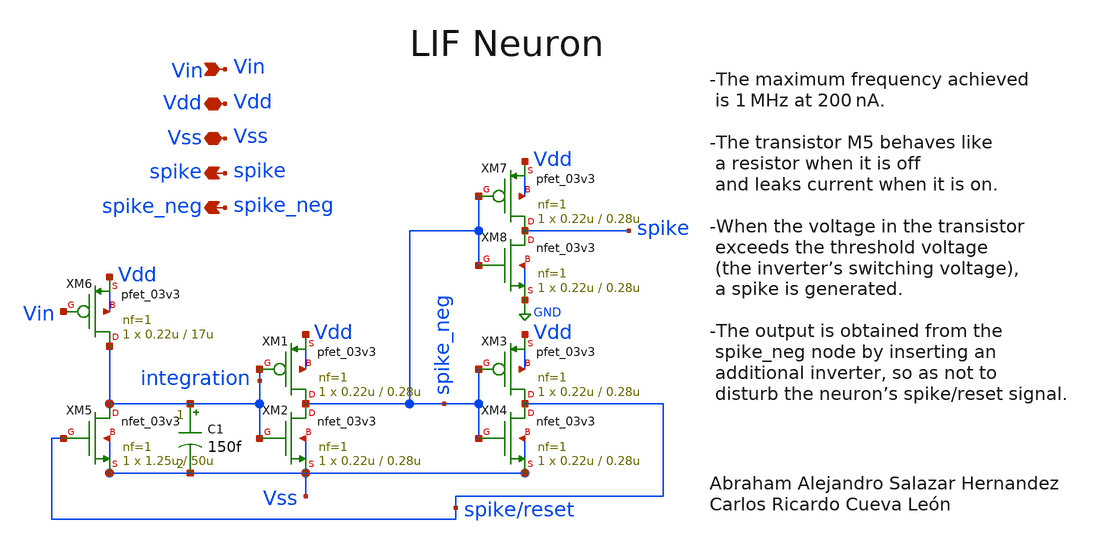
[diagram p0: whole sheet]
** sch_path: sch/lif/neurona.sch
**.subckt neurona Vdd Vss Vin spike spike_neg
*.iopin Vdd
*.iopin Vss
*.ipin Vin
*.opin spike
*.opin spike_neg
XM1 spike_neg integration Vdd Vdd pfet_03v3 L=0.28u W=0.22u nf=1 ad='int((nf+1)/2) * W/nf * 0.18u' as='int((nf+2)/2) * W/nf * 0.18u'
+ pd='2*int((nf+1)/2) * (W/nf + 0.18u)' ps='2*int((nf+2)/2) * (W/nf + 0.18u)' nrd='0.18u / W' nrs='0.18u / W'
+ sa=0 sb=0 sd=0 m=1
XM2 spike_neg integration Vss Vss nfet_03v3 L=0.28u W=0.22u nf=1 ad='int((nf+1)/2) * W/nf * 0.18u' as='int((nf+2)/2) * W/nf * 0.18u'
+ pd='2*int((nf+1)/2) * (W/nf + 0.18u)' ps='2*int((nf+2)/2) * (W/nf + 0.18u)' nrd='0.18u / W' nrs='0.18u / W'
+ sa=0 sb=0 sd=0 m=1
XM3 spike/reset spike_neg Vdd Vdd pfet_03v3 L=0.28u W=0.22u nf=1 ad='int((nf+1)/2) * W/nf * 0.18u' as='int((nf+2)/2) * W/nf * 0.18u'
+ pd='2*int((nf+1)/2) * (W/nf + 0.18u)' ps='2*int((nf+2)/2) * (W/nf + 0.18u)' nrd='0.18u / W' nrs='0.18u / W'
+ sa=0 sb=0 sd=0 m=1
XM4 spike/reset spike_neg Vss Vss nfet_03v3 L=0.28u W=0.22u nf=1 ad='int((nf+1)/2) * W/nf * 0.18u' as='int((nf+2)/2) * W/nf * 0.18u'
+ pd='2*int((nf+1)/2) * (W/nf + 0.18u)' ps='2*int((nf+2)/2) * (W/nf + 0.18u)' nrd='0.18u / W' nrs='0.18u / W'
+ sa=0 sb=0 sd=0 m=1
XM7 spike spike_neg Vdd Vdd pfet_03v3 L=0.28u W=0.22u nf=1 ad='int((nf+1)/2) * W/nf * 0.18u' as='int((nf+2)/2) * W/nf * 0.18u'
+ pd='2*int((nf+1)/2) * (W/nf + 0.18u)' ps='2*int((nf+2)/2) * (W/nf + 0.18u)' nrd='0.18u / W' nrs='0.18u / W'
+ sa=0 sb=0 sd=0 m=1
XM8 spike spike_neg GND GND nfet_03v3 L=0.28u W=0.22u nf=1 ad='int((nf+1)/2) * W/nf * 0.18u' as='int((nf+2)/2) * W/nf * 0.18u'
+ pd='2*int((nf+1)/2) * (W/nf + 0.18u)' ps='2*int((nf+2)/2) * (W/nf + 0.18u)' nrd='0.18u / W' nrs='0.18u / W'
+ sa=0 sb=0 sd=0 m=1
XM5 integration spike/reset Vss Vss nfet_03v3 L=50u W=1.25u nf=1 ad='int((nf+1)/2) * W/nf * 0.18u' as='int((nf+2)/2) * W/nf * 0.18u'
+ pd='2*int((nf+1)/2) * (W/nf + 0.18u)' ps='2*int((nf+2)/2) * (W/nf + 0.18u)' nrd='0.18u / W' nrs='0.18u / W'
+ sa=0 sb=0 sd=0 m=1
C1 integration Vss 150f m=1
XM6 integration Vin Vdd Vdd pfet_03v3 L=17u W=0.22u nf=1 ad='int((nf+1)/2) * W/nf * 0.18u' as='int((nf+2)/2) * W/nf * 0.18u'
+ pd='2*int((nf+1)/2) * (W/nf + 0.18u)' ps='2*int((nf+2)/2) * (W/nf + 0.18u)' nrd='0.18u / W' nrs='0.18u / W'
+ sa=0 sb=0 sd=0 m=1
**.ends
.GLOBAL GND
.end
